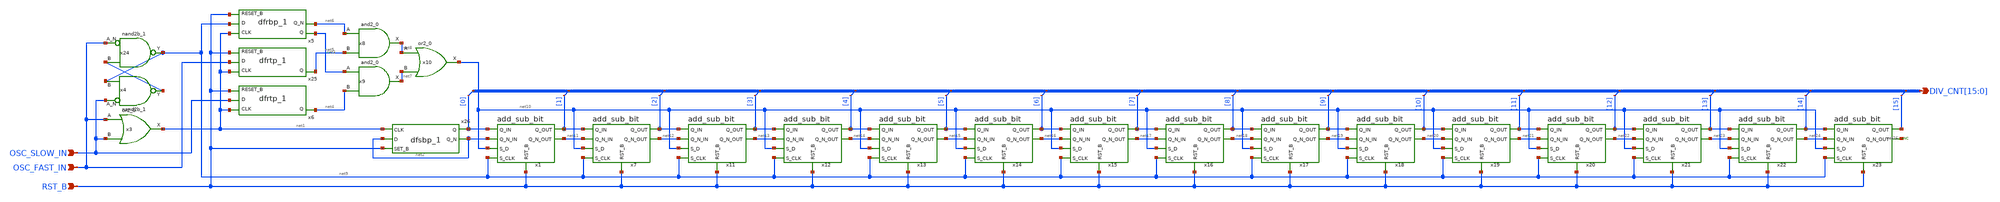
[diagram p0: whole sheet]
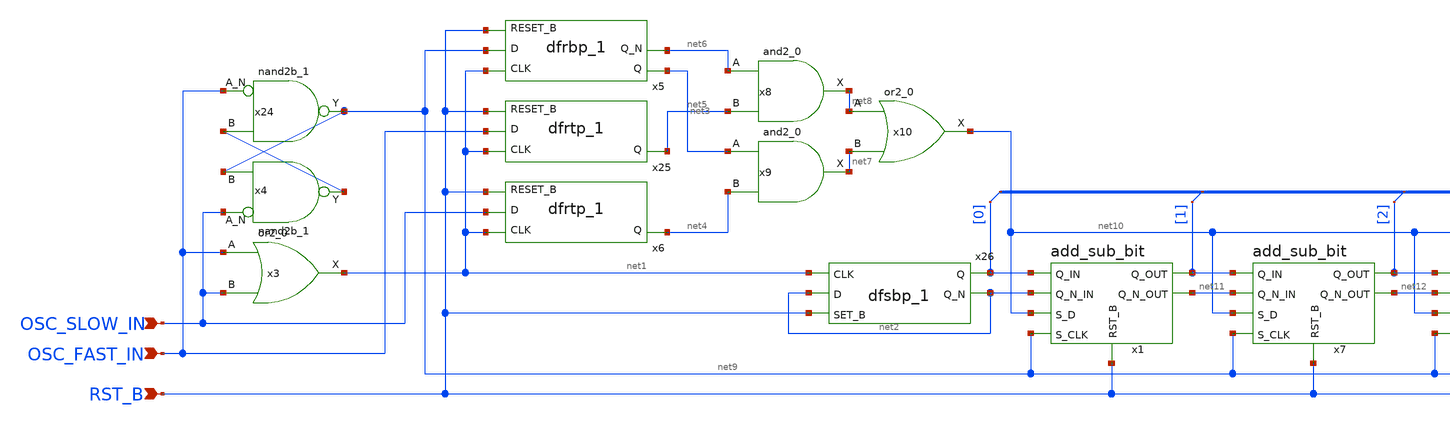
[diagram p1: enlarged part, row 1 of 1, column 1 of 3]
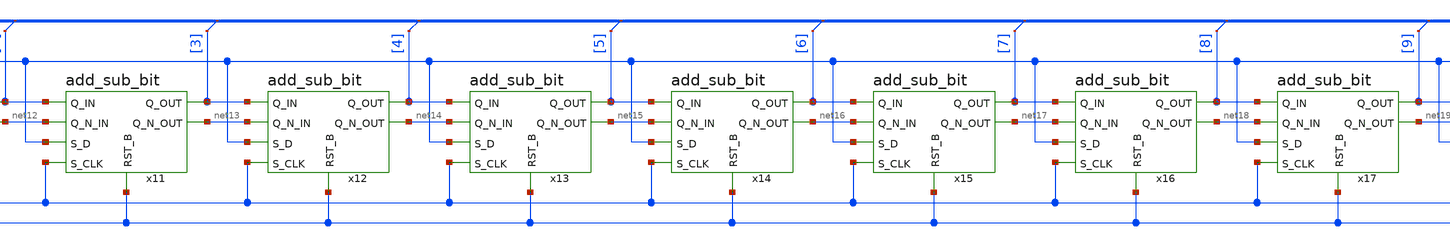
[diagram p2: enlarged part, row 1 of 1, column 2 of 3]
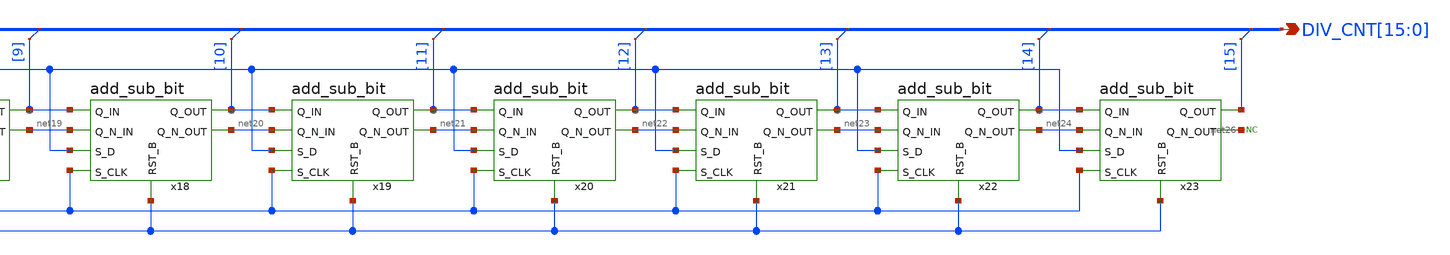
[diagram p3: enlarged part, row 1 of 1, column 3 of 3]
** sch_path: counter_inc_dec.sch
**.subckt counter_inc_dec OSC_FAST_IN OSC_SLOW_IN RST_B
*+ DIV_CNT[15],DIV_CNT[14],DIV_CNT[13],DIV_CNT[12],DIV_CNT[11],DIV_CNT[10],DIV_CNT[9],DIV_CNT[8],DIV_CNT[7],DIV_CNT[6],DIV_CNT[5],DIV_CNT[4],DIV_CNT[3],DIV_CNT[2],DIV_CNT[1],DIV_CNT[0]
*.ipin OSC_FAST_IN
*.ipin OSC_SLOW_IN
*.ipin RST_B
*.opin
*+ DIV_CNT[15],DIV_CNT[14],DIV_CNT[13],DIV_CNT[12],DIV_CNT[11],DIV_CNT[10],DIV_CNT[9],DIV_CNT[8],DIV_CNT[7],DIV_CNT[6],DIV_CNT[5],DIV_CNT[4],DIV_CNT[3],DIV_CNT[2],DIV_CNT[1],DIV_CNT[0]
x1 net11 net10 DIV_CNT[1] DIV_CNT[0] net2 net9 RST_B add_sub_bit
x3 OSC_FAST_IN OSC_SLOW_IN VGND VNB VPB VPWR net1 sky130_fd_sc_hd__or2_0
x5 net1 net9 RST_B VGND VNB VPB VPWR net3 net6 sky130_fd_sc_hd__dfrbp_1
x8 net6 net5 VGND VNB VPB VPWR net8 sky130_fd_sc_hd__and2_0
x9 net3 net4 VGND VNB VPB VPWR net7 sky130_fd_sc_hd__and2_0
x10 net8 net7 VGND VNB VPB VPWR net10 sky130_fd_sc_hd__or2_0
x25 net1 OSC_FAST_IN RST_B VGND VNB VPB VPWR net5 sky130_fd_sc_hd__dfrtp_1
x6 net1 OSC_SLOW_IN RST_B VGND VNB VPB VPWR net4 sky130_fd_sc_hd__dfrtp_1
x7 net12 net10 DIV_CNT[2] DIV_CNT[1] net11 net9 RST_B add_sub_bit
x11 net13 net10 DIV_CNT[3] DIV_CNT[2] net12 net9 RST_B add_sub_bit
x12 net14 net10 DIV_CNT[4] DIV_CNT[3] net13 net9 RST_B add_sub_bit
x13 net15 net10 DIV_CNT[5] DIV_CNT[4] net14 net9 RST_B add_sub_bit
x14 net16 net10 DIV_CNT[6] DIV_CNT[5] net15 net9 RST_B add_sub_bit
x15 net17 net10 DIV_CNT[7] DIV_CNT[6] net16 net9 RST_B add_sub_bit
x16 net18 net10 DIV_CNT[8] DIV_CNT[7] net17 net9 RST_B add_sub_bit
x17 net19 net10 DIV_CNT[9] DIV_CNT[8] net18 net9 RST_B add_sub_bit
x18 net20 net10 DIV_CNT[10] DIV_CNT[9] net19 net9 RST_B add_sub_bit
x19 net21 net10 DIV_CNT[11] DIV_CNT[10] net20 net9 RST_B add_sub_bit
x20 net22 net10 DIV_CNT[12] DIV_CNT[11] net21 net9 RST_B add_sub_bit
x21 net23 net10 DIV_CNT[13] DIV_CNT[12] net22 net9 RST_B add_sub_bit
x22 net24 net10 DIV_CNT[14] DIV_CNT[13] net23 net9 RST_B add_sub_bit
x23 net26 net10 DIV_CNT[15] DIV_CNT[14] net24 net9 RST_B add_sub_bit
* noconn #net26
x4 OSC_SLOW_IN net9 VGND VNB VPB VPWR net25 sky130_fd_sc_hd__nand2b_1
x24 OSC_FAST_IN net25 VGND VNB VPB VPWR net9 sky130_fd_sc_hd__nand2b_1
* tap: DIV_CNT[15:0] --> DIV_CNT[0]
* tap: DIV_CNT[15:0] --> DIV_CNT[1]
* tap: DIV_CNT[15:0] --> DIV_CNT[2]
* tap: DIV_CNT[15:0] --> DIV_CNT[3]
* tap: DIV_CNT[15:0] --> DIV_CNT[4]
* tap: DIV_CNT[15:0] --> DIV_CNT[5]
* tap: DIV_CNT[15:0] --> DIV_CNT[6]
* tap: DIV_CNT[15:0] --> DIV_CNT[7]
* tap: DIV_CNT[15:0] --> DIV_CNT[8]
* tap: DIV_CNT[15:0] --> DIV_CNT[9]
* tap: DIV_CNT[15:0] --> DIV_CNT[10]
* tap: DIV_CNT[15:0] --> DIV_CNT[11]
* tap: DIV_CNT[15:0] --> DIV_CNT[12]
* tap: DIV_CNT[15:0] --> DIV_CNT[13]
* tap: DIV_CNT[15:0] --> DIV_CNT[14]
* tap: DIV_CNT[15:0] --> DIV_CNT[15]
x26 net1 net2 RST_B VGND VNB VPB VPWR DIV_CNT[0] net2 sky130_fd_sc_hd__dfsbp_1
**.ends

* expanding   symbol:  add_sub_bit.sym # of pins=7
** sym_path: add_sub_bit.sym
** sch_path: add_sub_bit.sch
.subckt add_sub_bit Q_N_OUT S_D Q_OUT Q_IN Q_N_IN S_CLK RST_B
*.ipin S_D
*.ipin S_CLK
*.opin Q_OUT
*.opin Q_N_OUT
*.ipin RST_B
*.ipin Q_N_IN
*.ipin Q_IN
x2 Q_N_OUT Q_OUT S_D VGND VNB VPB VPWR net2 sky130_fd_sc_hd__mux2_1
x3 Q_IN Q_N_IN S_CLK VGND VNB VPB VPWR net1 sky130_fd_sc_hd__mux2_1
x4 net1 net2 RST_B VGND VNB VPB VPWR Q_OUT Q_N_OUT sky130_fd_sc_hd__dfrbp_1
.ends

.end
